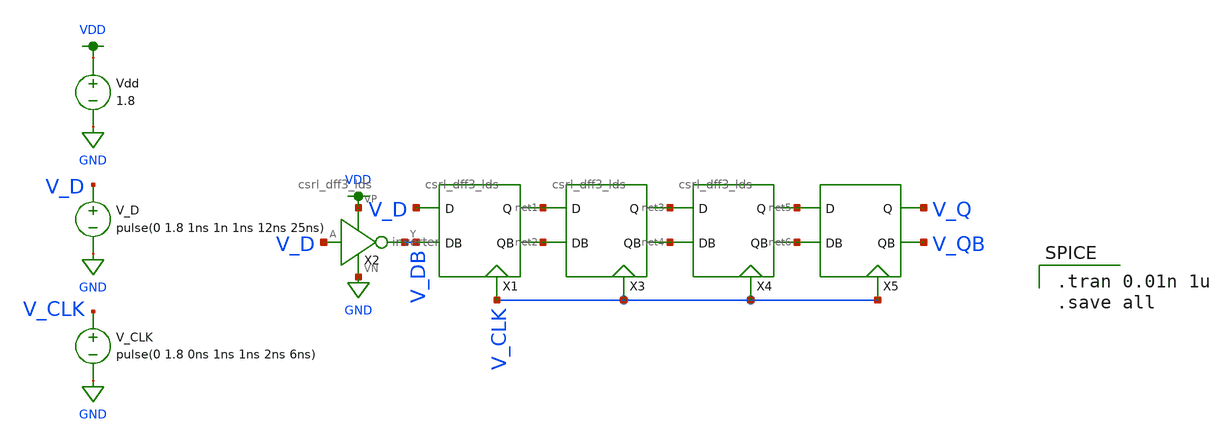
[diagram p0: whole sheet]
** sch_path: MP2/xschem/final/4reg_tran.sch
**.subckt 4reg_tran
X2 V_D V_DB VDD GND inverter
Vdd VDD GND 1.8
V_D V_D GND pulse(0 1.8 1ns 1n 1ns 12ns 25ns)
V_CLK V_CLK GND pulse(0 1.8 0ns 1ns 1ns 2ns 6ns)
X1 V_D V_DB net1 net2 V_CLK csrl_dff3_lds
X3 net1 net2 net3 net4 V_CLK csrl_dff3_lds
X4 net3 net4 net5 net6 V_CLK csrl_dff3_lds
X5 net5 net6 V_Q V_QB V_CLK csrl_dff3_lds
**** begin user architecture code

.tran 0.01n 1u
.save all


.option wnflag=1
.lib ~/skywater/skywater-pdk/libraries/sky130_fd_pr_ngspice/latest/models/sky130.lib.spice sf

**** end user architecture code
**.ends
.GLOBAL GND
.GLOBAL VDD
.end
